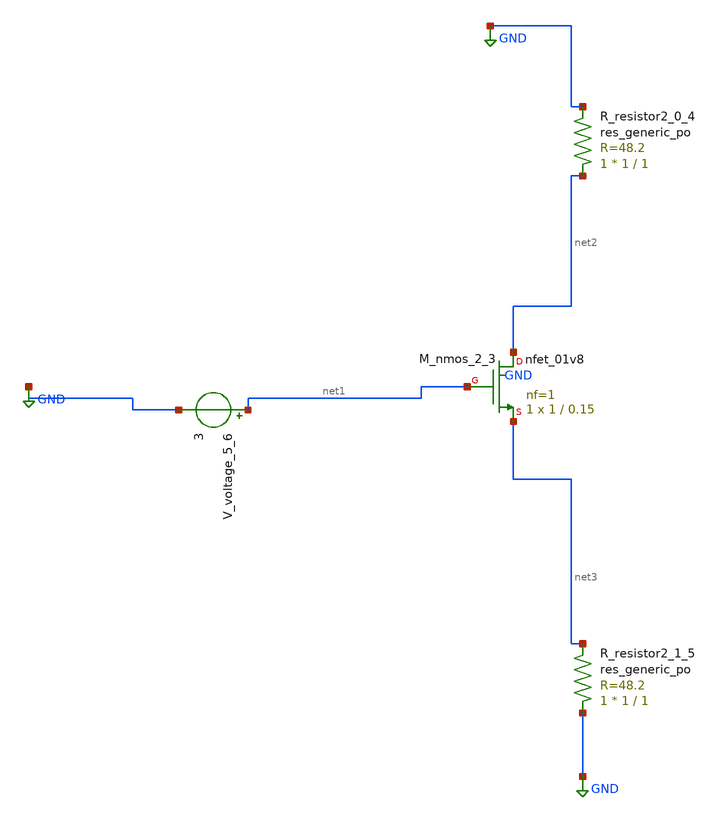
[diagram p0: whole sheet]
** sch_path: schematics/AMSNet/456.sch
**.subckt 456
XM_nmos_2_3 net2 net1 net3 GND sky130_fd_pr__nfet_01v8 L=0.15 W=1 nf=1 ad='int((1 + 1)/2) * 1 / 1 * 0.29'
+ as='int((1 + 2)/2) * 1 / 1 * 0.29' pd='2*int((1 + 1)/2) * (1 / 1 + 0.29)' ps='2*int((1 + 2)/2) * (1 / 1 + 0.29)'
+ nrd='0.29 / 1 ' nrs='0.29 / 1 ' sa=0 sb=0 sd=0 mult=1 m=1
XR_resistor2_0_4 net2 GND sky130_fd_pr__res_generic_po W=1 L=1 m=1
XR_resistor2_1_5 GND net3 sky130_fd_pr__res_generic_po W=1 L=1 m=1
V_voltage_5_6 net1 GND 3
**.ends
.GLOBAL GND
.end
